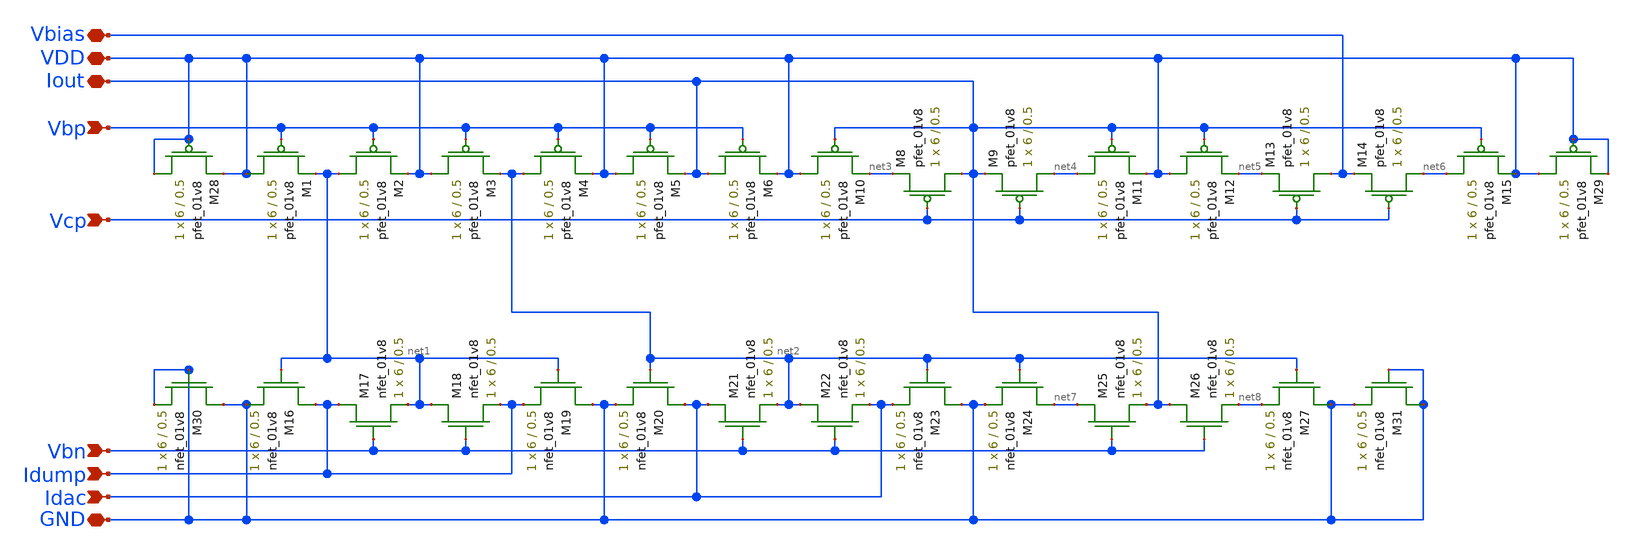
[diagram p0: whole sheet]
** sch_path: schematics/ieee DAC/LDS_Output_stage.sch
**.subckt LDS_Output_stage VDD Idump Iout Idac GND Vbias Vbp Vcp Vbn
*.iopin VDD
*.ipin Idump
*.iopin Iout
*.ipin Idac
*.iopin GND
*.iopin Vbias
*.ipin Vbp
*.ipin Vcp
*.ipin Vbn
XM1 VDD Vbp net1 VDD sky130_fd_pr__pfet_01v8 L=0.5 W=6 nf=1 ad='int((nf+1)/2) * W/nf * 0.29' as='int((nf+2)/2) * W/nf * 0.29'
+ pd='2*int((nf+1)/2) * (W/nf + 0.29)' ps='2*int((nf+2)/2) * (W/nf + 0.29)' nrd='0.29 / W' nrs='0.29 / W'
+ sa=0 sb=0 sd=0 mult=1 m=1
XM2 net1 Vbp VDD VDD sky130_fd_pr__pfet_01v8 L=0.5 W=6 nf=1 ad='int((nf+1)/2) * W/nf * 0.29' as='int((nf+2)/2) * W/nf * 0.29'
+ pd='2*int((nf+1)/2) * (W/nf + 0.29)' ps='2*int((nf+2)/2) * (W/nf + 0.29)' nrd='0.29 / W' nrs='0.29 / W'
+ sa=0 sb=0 sd=0 mult=1 m=1
XM3 VDD Vbp net2 VDD sky130_fd_pr__pfet_01v8 L=0.5 W=6 nf=1 ad='int((nf+1)/2) * W/nf * 0.29' as='int((nf+2)/2) * W/nf * 0.29'
+ pd='2*int((nf+1)/2) * (W/nf + 0.29)' ps='2*int((nf+2)/2) * (W/nf + 0.29)' nrd='0.29 / W' nrs='0.29 / W'
+ sa=0 sb=0 sd=0 mult=1 m=1
XM4 net2 Vbp VDD VDD sky130_fd_pr__pfet_01v8 L=0.5 W=6 nf=1 ad='int((nf+1)/2) * W/nf * 0.29' as='int((nf+2)/2) * W/nf * 0.29'
+ pd='2*int((nf+1)/2) * (W/nf + 0.29)' ps='2*int((nf+2)/2) * (W/nf + 0.29)' nrd='0.29 / W' nrs='0.29 / W'
+ sa=0 sb=0 sd=0 mult=1 m=1
XM5 VDD Vbp Iout VDD sky130_fd_pr__pfet_01v8 L=0.5 W=6 nf=1 ad='int((nf+1)/2) * W/nf * 0.29' as='int((nf+2)/2) * W/nf * 0.29'
+ pd='2*int((nf+1)/2) * (W/nf + 0.29)' ps='2*int((nf+2)/2) * (W/nf + 0.29)' nrd='0.29 / W' nrs='0.29 / W'
+ sa=0 sb=0 sd=0 mult=1 m=1
XM6 Iout Vbp VDD VDD sky130_fd_pr__pfet_01v8 L=0.5 W=6 nf=1 ad='int((nf+1)/2) * W/nf * 0.29' as='int((nf+2)/2) * W/nf * 0.29'
+ pd='2*int((nf+1)/2) * (W/nf + 0.29)' ps='2*int((nf+2)/2) * (W/nf + 0.29)' nrd='0.29 / W' nrs='0.29 / W'
+ sa=0 sb=0 sd=0 mult=1 m=1
XM8 Iout Vcp net3 VDD sky130_fd_pr__pfet_01v8 L=0.5 W=6 nf=1 ad='int((nf+1)/2) * W/nf * 0.29' as='int((nf+2)/2) * W/nf * 0.29'
+ pd='2*int((nf+1)/2) * (W/nf + 0.29)' ps='2*int((nf+2)/2) * (W/nf + 0.29)' nrd='0.29 / W' nrs='0.29 / W'
+ sa=0 sb=0 sd=0 mult=1 m=1
XM9 net4 Vcp Iout VDD sky130_fd_pr__pfet_01v8 L=0.5 W=6 nf=1 ad='int((nf+1)/2) * W/nf * 0.29' as='int((nf+2)/2) * W/nf * 0.29'
+ pd='2*int((nf+1)/2) * (W/nf + 0.29)' ps='2*int((nf+2)/2) * (W/nf + 0.29)' nrd='0.29 / W' nrs='0.29 / W'
+ sa=0 sb=0 sd=0 mult=1 m=1
XM10 VDD Iout net3 VDD sky130_fd_pr__pfet_01v8 L=0.5 W=6 nf=1 ad='int((nf+1)/2) * W/nf * 0.29' as='int((nf+2)/2) * W/nf * 0.29'
+ pd='2*int((nf+1)/2) * (W/nf + 0.29)' ps='2*int((nf+2)/2) * (W/nf + 0.29)' nrd='0.29 / W' nrs='0.29 / W'
+ sa=0 sb=0 sd=0 mult=1 m=1
XM11 net4 Iout VDD VDD sky130_fd_pr__pfet_01v8 L=0.5 W=6 nf=1 ad='int((nf+1)/2) * W/nf * 0.29' as='int((nf+2)/2) * W/nf * 0.29'
+ pd='2*int((nf+1)/2) * (W/nf + 0.29)' ps='2*int((nf+2)/2) * (W/nf + 0.29)' nrd='0.29 / W' nrs='0.29 / W'
+ sa=0 sb=0 sd=0 mult=1 m=1
XM12 VDD Iout net5 VDD sky130_fd_pr__pfet_01v8 L=0.5 W=6 nf=1 ad='int((nf+1)/2) * W/nf * 0.29' as='int((nf+2)/2) * W/nf * 0.29'
+ pd='2*int((nf+1)/2) * (W/nf + 0.29)' ps='2*int((nf+2)/2) * (W/nf + 0.29)' nrd='0.29 / W' nrs='0.29 / W'
+ sa=0 sb=0 sd=0 mult=1 m=1
XM13 Vbias Vcp net5 VDD sky130_fd_pr__pfet_01v8 L=0.5 W=6 nf=1 ad='int((nf+1)/2) * W/nf * 0.29' as='int((nf+2)/2) * W/nf * 0.29'
+ pd='2*int((nf+1)/2) * (W/nf + 0.29)' ps='2*int((nf+2)/2) * (W/nf + 0.29)' nrd='0.29 / W' nrs='0.29 / W'
+ sa=0 sb=0 sd=0 mult=1 m=1
XM14 net6 Vcp Vbias VDD sky130_fd_pr__pfet_01v8 L=0.5 W=6 nf=1 ad='int((nf+1)/2) * W/nf * 0.29' as='int((nf+2)/2) * W/nf * 0.29'
+ pd='2*int((nf+1)/2) * (W/nf + 0.29)' ps='2*int((nf+2)/2) * (W/nf + 0.29)' nrd='0.29 / W' nrs='0.29 / W'
+ sa=0 sb=0 sd=0 mult=1 m=1
XM15 net6 Iout VDD VDD sky130_fd_pr__pfet_01v8 L=0.5 W=6 nf=1 ad='int((nf+1)/2) * W/nf * 0.29' as='int((nf+2)/2) * W/nf * 0.29'
+ pd='2*int((nf+1)/2) * (W/nf + 0.29)' ps='2*int((nf+2)/2) * (W/nf + 0.29)' nrd='0.29 / W' nrs='0.29 / W'
+ sa=0 sb=0 sd=0 mult=1 m=1
XM16 Idump net1 GND GND sky130_fd_pr__nfet_01v8 L=0.5 W=6 nf=1 ad='int((nf+1)/2) * W/nf * 0.29' as='int((nf+2)/2) * W/nf * 0.29'
+ pd='2*int((nf+1)/2) * (W/nf + 0.29)' ps='2*int((nf+2)/2) * (W/nf + 0.29)' nrd='0.29 / W' nrs='0.29 / W'
+ sa=0 sb=0 sd=0 mult=1 m=1
XM17 Idump Vbn net1 GND sky130_fd_pr__nfet_01v8 L=0.5 W=6 nf=1 ad='int((nf+1)/2) * W/nf * 0.29' as='int((nf+2)/2) * W/nf * 0.29'
+ pd='2*int((nf+1)/2) * (W/nf + 0.29)' ps='2*int((nf+2)/2) * (W/nf + 0.29)' nrd='0.29 / W' nrs='0.29 / W'
+ sa=0 sb=0 sd=0 mult=1 m=1
XM18 net1 Vbn Idump GND sky130_fd_pr__nfet_01v8 L=0.5 W=6 nf=1 ad='int((nf+1)/2) * W/nf * 0.29' as='int((nf+2)/2) * W/nf * 0.29'
+ pd='2*int((nf+1)/2) * (W/nf + 0.29)' ps='2*int((nf+2)/2) * (W/nf + 0.29)' nrd='0.29 / W' nrs='0.29 / W'
+ sa=0 sb=0 sd=0 mult=1 m=1
XM19 GND net1 Idump GND sky130_fd_pr__nfet_01v8 L=0.5 W=6 nf=1 ad='int((nf+1)/2) * W/nf * 0.29' as='int((nf+2)/2) * W/nf * 0.29'
+ pd='2*int((nf+1)/2) * (W/nf + 0.29)' ps='2*int((nf+2)/2) * (W/nf + 0.29)' nrd='0.29 / W' nrs='0.29 / W'
+ sa=0 sb=0 sd=0 mult=1 m=1
XM20 Idac net2 GND GND sky130_fd_pr__nfet_01v8 L=0.5 W=6 nf=1 ad='int((nf+1)/2) * W/nf * 0.29' as='int((nf+2)/2) * W/nf * 0.29'
+ pd='2*int((nf+1)/2) * (W/nf + 0.29)' ps='2*int((nf+2)/2) * (W/nf + 0.29)' nrd='0.29 / W' nrs='0.29 / W'
+ sa=0 sb=0 sd=0 mult=1 m=1
XM21 Idac Vbn net2 GND sky130_fd_pr__nfet_01v8 L=0.5 W=6 nf=1 ad='int((nf+1)/2) * W/nf * 0.29' as='int((nf+2)/2) * W/nf * 0.29'
+ pd='2*int((nf+1)/2) * (W/nf + 0.29)' ps='2*int((nf+2)/2) * (W/nf + 0.29)' nrd='0.29 / W' nrs='0.29 / W'
+ sa=0 sb=0 sd=0 mult=1 m=1
XM22 net2 Vbn Idac GND sky130_fd_pr__nfet_01v8 L=0.5 W=6 nf=1 ad='int((nf+1)/2) * W/nf * 0.29' as='int((nf+2)/2) * W/nf * 0.29'
+ pd='2*int((nf+1)/2) * (W/nf + 0.29)' ps='2*int((nf+2)/2) * (W/nf + 0.29)' nrd='0.29 / W' nrs='0.29 / W'
+ sa=0 sb=0 sd=0 mult=1 m=1
XM23 GND net2 Idac GND sky130_fd_pr__nfet_01v8 L=0.5 W=6 nf=1 ad='int((nf+1)/2) * W/nf * 0.29' as='int((nf+2)/2) * W/nf * 0.29'
+ pd='2*int((nf+1)/2) * (W/nf + 0.29)' ps='2*int((nf+2)/2) * (W/nf + 0.29)' nrd='0.29 / W' nrs='0.29 / W'
+ sa=0 sb=0 sd=0 mult=1 m=1
XM24 net7 net2 GND GND sky130_fd_pr__nfet_01v8 L=0.5 W=6 nf=1 ad='int((nf+1)/2) * W/nf * 0.29' as='int((nf+2)/2) * W/nf * 0.29'
+ pd='2*int((nf+1)/2) * (W/nf + 0.29)' ps='2*int((nf+2)/2) * (W/nf + 0.29)' nrd='0.29 / W' nrs='0.29 / W'
+ sa=0 sb=0 sd=0 mult=1 m=1
XM25 net7 Vbn Iout GND sky130_fd_pr__nfet_01v8 L=0.5 W=6 nf=1 ad='int((nf+1)/2) * W/nf * 0.29' as='int((nf+2)/2) * W/nf * 0.29'
+ pd='2*int((nf+1)/2) * (W/nf + 0.29)' ps='2*int((nf+2)/2) * (W/nf + 0.29)' nrd='0.29 / W' nrs='0.29 / W'
+ sa=0 sb=0 sd=0 mult=1 m=1
XM26 Iout Vbn net8 GND sky130_fd_pr__nfet_01v8 L=0.5 W=6 nf=1 ad='int((nf+1)/2) * W/nf * 0.29' as='int((nf+2)/2) * W/nf * 0.29'
+ pd='2*int((nf+1)/2) * (W/nf + 0.29)' ps='2*int((nf+2)/2) * (W/nf + 0.29)' nrd='0.29 / W' nrs='0.29 / W'
+ sa=0 sb=0 sd=0 mult=1 m=1
XM27 GND net2 net8 GND sky130_fd_pr__nfet_01v8 L=0.5 W=6 nf=1 ad='int((nf+1)/2) * W/nf * 0.29' as='int((nf+2)/2) * W/nf * 0.29'
+ pd='2*int((nf+1)/2) * (W/nf + 0.29)' ps='2*int((nf+2)/2) * (W/nf + 0.29)' nrd='0.29 / W' nrs='0.29 / W'
+ sa=0 sb=0 sd=0 mult=1 m=1
XM28 VDD VDD VDD VDD sky130_fd_pr__pfet_01v8 L=0.5 W=6 nf=1 ad='int((nf+1)/2) * W/nf * 0.29' as='int((nf+2)/2) * W/nf * 0.29'
+ pd='2*int((nf+1)/2) * (W/nf + 0.29)' ps='2*int((nf+2)/2) * (W/nf + 0.29)' nrd='0.29 / W' nrs='0.29 / W'
+ sa=0 sb=0 sd=0 mult=1 m=1
XM29 VDD VDD VDD VDD sky130_fd_pr__pfet_01v8 L=0.5 W=6 nf=1 ad='int((nf+1)/2) * W/nf * 0.29' as='int((nf+2)/2) * W/nf * 0.29'
+ pd='2*int((nf+1)/2) * (W/nf + 0.29)' ps='2*int((nf+2)/2) * (W/nf + 0.29)' nrd='0.29 / W' nrs='0.29 / W'
+ sa=0 sb=0 sd=0 mult=1 m=1
XM30 GND GND GND GND sky130_fd_pr__nfet_01v8 L=0.5 W=6 nf=1 ad='int((nf+1)/2) * W/nf * 0.29' as='int((nf+2)/2) * W/nf * 0.29'
+ pd='2*int((nf+1)/2) * (W/nf + 0.29)' ps='2*int((nf+2)/2) * (W/nf + 0.29)' nrd='0.29 / W' nrs='0.29 / W'
+ sa=0 sb=0 sd=0 mult=1 m=1
XM31 GND GND GND GND sky130_fd_pr__nfet_01v8 L=0.5 W=6 nf=1 ad='int((nf+1)/2) * W/nf * 0.29' as='int((nf+2)/2) * W/nf * 0.29'
+ pd='2*int((nf+1)/2) * (W/nf + 0.29)' ps='2*int((nf+2)/2) * (W/nf + 0.29)' nrd='0.29 / W' nrs='0.29 / W'
+ sa=0 sb=0 sd=0 mult=1 m=1
**.ends
.end
